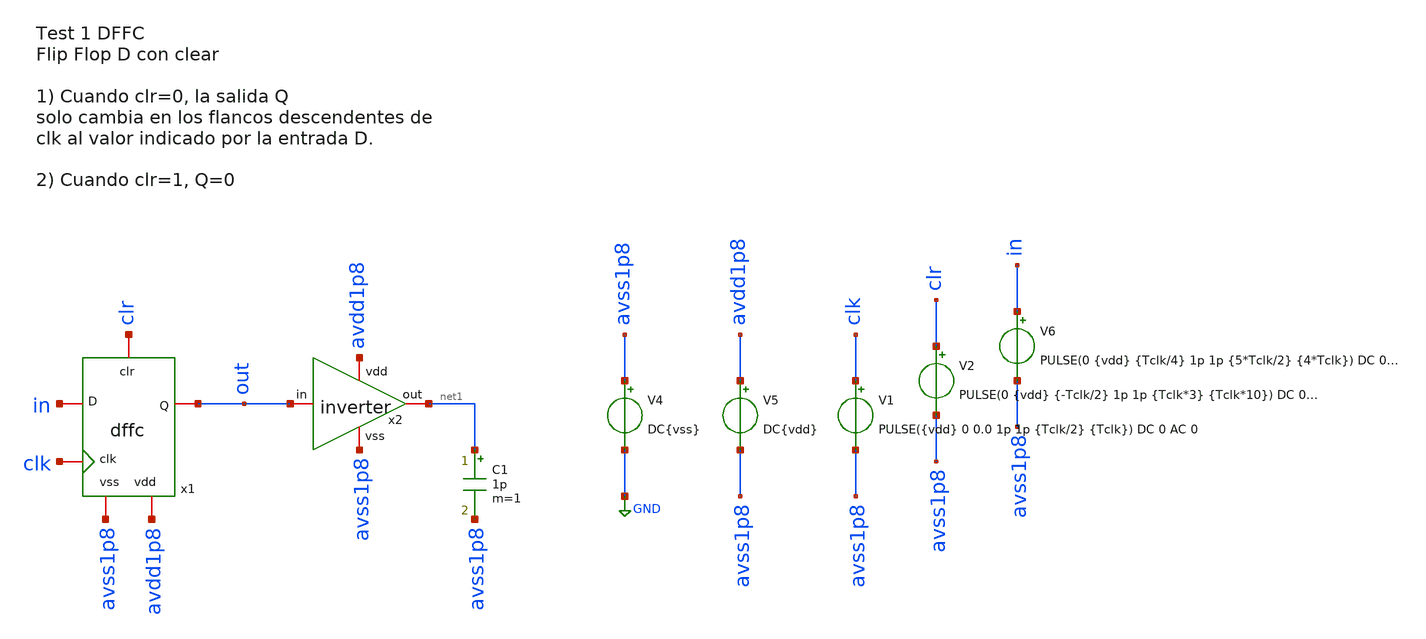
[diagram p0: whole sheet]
** sch_path: designs/sch/tests/test1_dffc.sch
**.subckt test1_dffc
x2 avdd1p8 net1 out avss1p8 inverter
V4 avss1p8 GND DC{vss}
V5 avdd1p8 avss1p8 DC{vdd}
V6 in avss1p8 PULSE(0 {vdd} {Tclk/4} 1p 1p {5*Tclk/2} {4*Tclk}) DC 0 AC 0
C1 net1 avss1p8 1p m=1
x1 out in clk clr avss1p8 avdd1p8 dffc
V1 clk avss1p8 PULSE({vdd} 0 0.0 1p 1p {Tclk/2} {Tclk}) DC 0 AC 0
V2 clr avss1p8 PULSE(0 {vdd} {-Tclk/2} 1p 1p {Tclk*3} {Tclk*10}) DC 0 AC 0
**** begin user architecture code


* Circuit Parameters
.param vdd = 1.8
.param vss = 0.0
.param Tclk = 10n
.options TEMP = 65.0

* Include Models
.lib /foss/pdks/sky130A/libs.tech/ngspice/sky130.lib.spice TT

* OP Parameters & Singals to save
.save all

* Simulations
.control
  tran 0.01u 240n
  setplot tran1
  plot clr v(in)+2 v(out)+4 clk+6
reset
.endc

.end


**** end user architecture code
**.ends
.GLOBAL GND
.end
